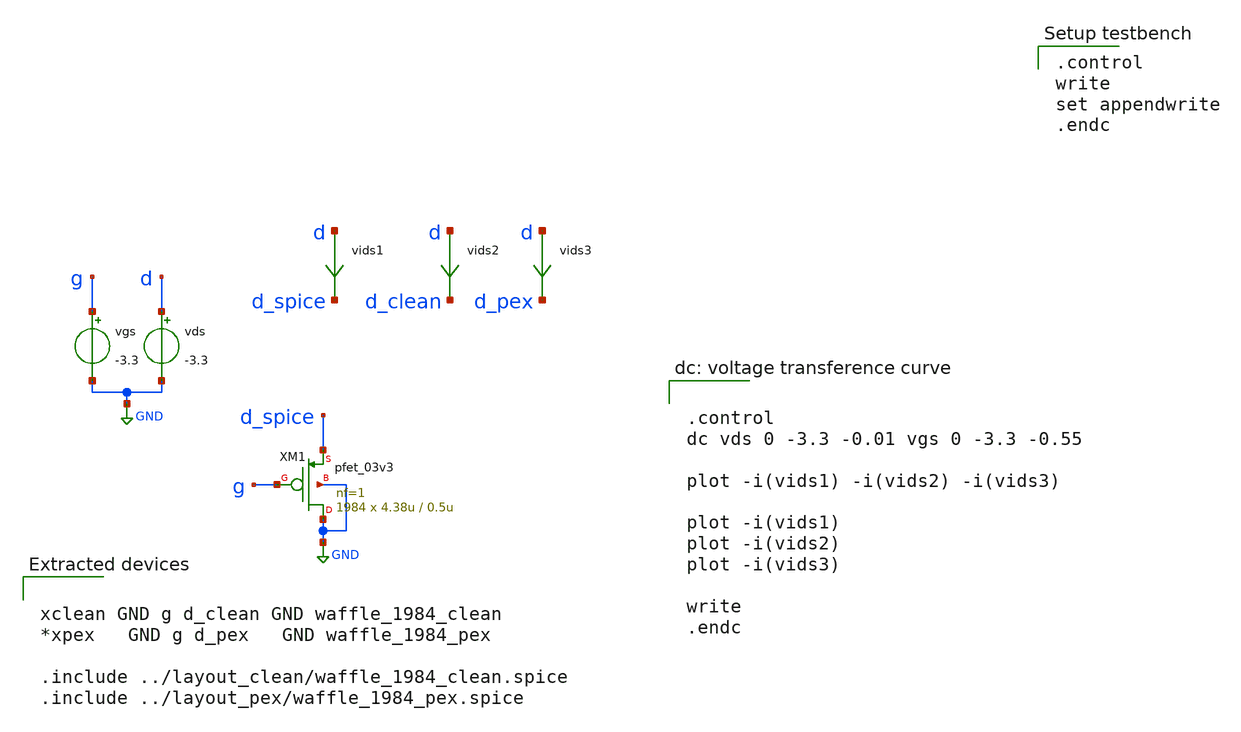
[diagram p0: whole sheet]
** sch_path: LDO/xschem/waffle_1984/test/charac_pex.sch
 .control
write
set appendwrite
.endc

.include $env(PDK_ROOT)/$env(PDK)/libs.tech/ngspice/design.ngspice
.lib $env(PDK_ROOT)/$env(PDK)/libs.tech/ngspice/sm141064.ngspice typical
.lib $env(PDK_ROOT)/$env(PDK)/libs.tech/ngspice/sm141064.ngspice mimcap_statistical
.lib $env(PDK_ROOT)/$env(PDK)/libs.tech/ngspice/sm141064.ngspice cap_mim
.lib $env(PDK_ROOT)/$env(PDK)/libs.tech/ngspice/sm141064.ngspice res_typical
.lib $env(PDK_ROOT)/$env(PDK)/libs.tech/ngspice/sm141064.ngspice bjt_typical
.lib $env(PDK_ROOT)/$env(PDK)/libs.tech/ngspice/sm141064.ngspice moscap_typical

**.subckt charac_pex
vgs g GND -3.3
vds d GND -3.3
vids1 d d_spice 0
.save i(vids1)
vids2 d d_clean 0
.save i(vids2)
XM1 GND g d_spice GND pfet_03v3 L=0.5u W=4.38u nf=1 ad='int((nf+1)/2) * W/nf * 0.18u' as='int((nf+2)/2) * W/nf * 0.18u'
+ pd='2*int((nf+1)/2) * (W/nf + 0.18u)' ps='2*int((nf+2)/2) * (W/nf + 0.18u)' nrd='0.18u / W' nrs='0.18u / W'
+ sa=0 sb=0 sd=0 m=1984
vids3 d d_pex 0
.save i(vids3)
**** begin user architecture code


.control
dc vds 0 -3.3 -0.01 vgs 0 -3.3 -0.55

plot -i(vids1) -i(vids2) -i(vids3)

plot -i(vids1)
plot -i(vids2)
plot -i(vids3)

write
.endc




xclean GND g d_clean GND waffle_1984_clean
*xpex   GND g d_pex   GND waffle_1984_pex

.include ../layout_clean/waffle_1984_clean.spice
.include ../layout_pex/waffle_1984_pex.spice


**** end user architecture code
**.ends
.GLOBAL GND
.end
